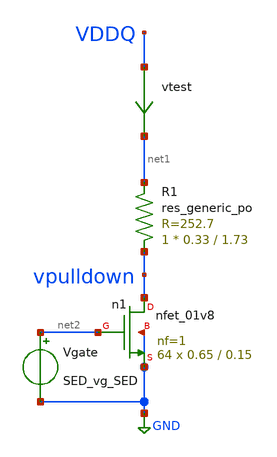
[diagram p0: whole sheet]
** sch_path: test_resistance.sch
* Copyright 2021 Stefan Frederik Schippers
* Licensed under the Apache License, Version 2.0 (the "License");
* you may not use this file except in compliance with the License.
* You may obtain a copy of the License at
* https://www.apache.org/licenses/LICENSE-2.0
* Unless required by applicable law or agreed to in writing, software
* distributed under the License is distributed on an "AS IS" BASIS,
* WITHOUT WARRANTIES OR CONDITIONS OF ANY KIND, either express or implied.
* See the License for the specific language governing permissions and
* limitations under the License.
**.subckt test_resistance
XR1 vpulldown net1 sky130_fd_pr__res_generic_po W=0.33 L=1.73 m=1
vtest VDDQ net1 0
.save i(vtest)
Xn1 vpulldown net2 GND GND sky130_fd_pr__nfet_01v8 L=0.15 W=0.65 nf=1 ad='int((nf+1)/2) * W/nf * 0.29'
+ as='int((nf+2)/2) * W/nf * 0.29' pd='2*int((nf+1)/2) * (W/nf + 0.29)' ps='2*int((nf+2)/2) * (W/nf + 0.29)'
+ nrd='0.29 / W' nrs='0.29 / W' sa=0 sb=0 sd=0 mult=64 m=64
Vgate net2 GND SED_vg_SED
**** begin user architecture code
 ** Local library links to pdk
.lib ./libs/SED_process_SED_lib.spice SED_process_SED

**** end user architecture code
**.ends
.GLOBAL GND
**** begin user architecture code



* power voltage
vvddq VDDQ 0 0
*.param rwidth=4.6

.control
save all
set temp=SED_temp_SED

* RUN SIMULATION
dc vvddq 0.1 1.65 0.05
* OUTPUT
*plot vddq/I(vtest) vs vddq
*MEAS DC r_max MAX par('vddq/I(vtest)')
print v(vddq)/i(vtest)
set hcopydevtype = svg
hardcopy ./out/plots/SED_plotName_SED.svg vddq/I(vtest) vs vddq title 'Resistance vs pin voltage'

.endc


**** end user architecture code
.end
